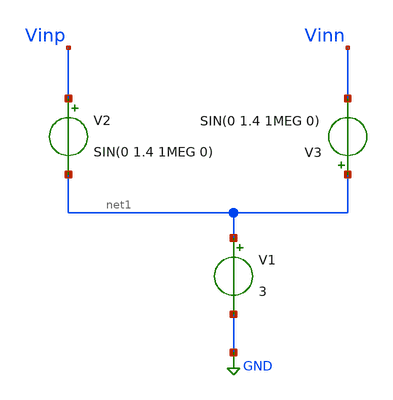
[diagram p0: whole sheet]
** sch_path: SAR_ADC/tracking_switches/xschem/test_sources.sch
**.subckt test_sources
V1 net1 GND 3
V2 Vinp net1 SIN(0 1.4 1MEG 0)
V3 net1 Vinn SIN(0 1.4 1MEG 0)
**** begin user architecture code



*Parameters

.options TEMP = 50.0
.lib /home/gf180/Documents/gf180/pdk/gf180mcuD/libs.tech/ngspice/sm141064.ngspice typical
.include /home/gf180/Documents/gf180/pdk/gf180mcuD/libs.tech/ngspice/design.ngspice
.lib /home/gf180/Documents/gf180/pdk/gf180mcuD/libs.tech/ngspice/sm141064.ngspice cap_mim
.lib /home/gf180/Documents/gf180/pdk/gf180mcuD/libs.tech/ngspice/sm141064.ngspice mimcap_statistical

*Data to save

.save V(Vinp)
.save V(Vinn)

* Simulation
.control
tran 5n 10u
.option method=gear reltol=1e-6 interp

*setplot dc1
let vin_diff = V(Vinp) - V(Vinn)
plot vin_diff V(Vinp) V(Vinn)

wrdata output.txt clks vin_diff vout_diff

reset
unset filetype
op
save all
write tracking_switches_tb.raw


.endc
.end


**** end user architecture code
**.ends
.GLOBAL GND
.end
